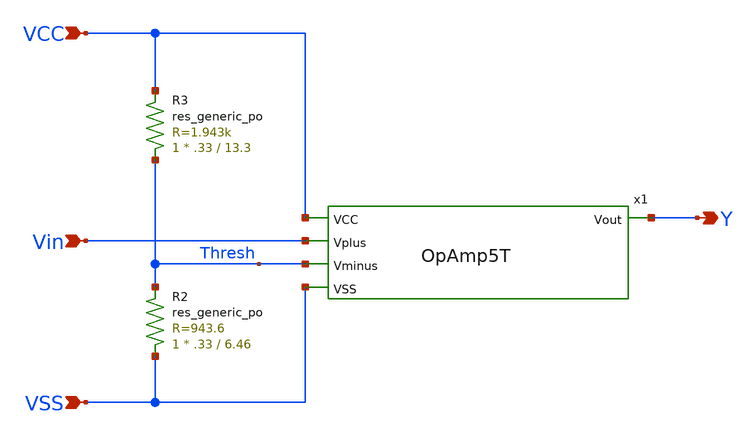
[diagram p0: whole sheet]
** sch_path: xschem/oneBitADC.sch
**.subckt oneBitADC VCC VSS Vin Y
*.ipin VCC
*.ipin VSS
*.ipin Vin
*.opin Y
XR3 Thresh VCC sky130_fd_pr__res_generic_po W=.33 L=13.3 m=1
XR2 VSS Thresh sky130_fd_pr__res_generic_po W=.33 L=6.46 m=1
x1 VCC Y Vin Thresh VSS OpAmp5T
**.ends

* expanding   symbol:  OpAmp5T.sym # of pins=5
** sym_path: xschem/OpAmp5T.sym
** sch_path: xschem/OpAmp5T.sch
.subckt OpAmp5T VCC Vout Vplus Vminus VSS
*.ipin VCC
*.ipin VSS
*.ipin Vplus
*.ipin Vminus
*.opin Vout
XM5 Vout net1 VCC VCC sky130_fd_pr__pfet_01v8_lvt L=2 W=8 nf=1 ad='W * 0.29' as='W * 0.29' pd='2*(W + 0.29)'
+ ps='2*(W + 0.29)' nrd=0 nrs=0 sa=0 sb=0 sd=0 mult=1 m=1
XM6 net1 net1 VCC VCC sky130_fd_pr__pfet_01v8_lvt L=2 W=8 nf=1 ad='W * 0.29' as='W * 0.29' pd='2*(W + 0.29)'
+ ps='2*(W + 0.29)' nrd=0 nrs=0 sa=0 sb=0 sd=0 mult=1 m=1
XM17 SN VCC VSS VSS sky130_fd_pr__nfet_01v8_lvt L=2 W=6 nf=1 ad='W * 0.29' as='W * 0.29' pd='2*(W + 0.29)'
+ ps='2*(W + 0.29)' nrd=0 nrs=0 sa=0 sb=0 sd=0 mult=1 m=1
XM23 Vout Vminus SN VSS sky130_fd_pr__nfet_01v8 L=2 W=4 nf=1 ad='W * 0.29' as='W * 0.29' pd='2*(W + 0.29)'
+ ps='2*(W + 0.29)' nrd=0 nrs=0 sa=0 sb=0 sd=0 mult=1 m=1
XM16 net1 Vplus SN VSS sky130_fd_pr__nfet_01v8 L=2 W=4 nf=1 ad='W * 0.29' as='W * 0.29' pd='2*(W + 0.29)'
+ ps='2*(W + 0.29)' nrd=0 nrs=0 sa=0 sb=0 sd=0 mult=1 m=1
.ends

.end
